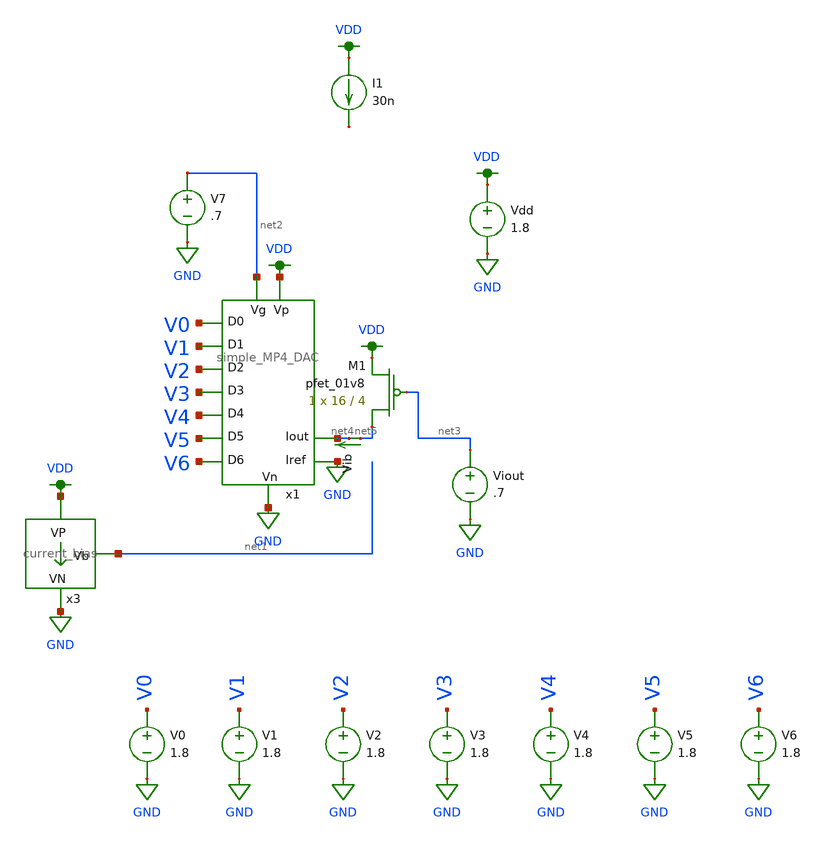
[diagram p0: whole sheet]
** sch_path: Final DAC files/schematics/simulations/DAC_mc_simulation.sch
**.subckt DAC_mc_simulation
Vdd VDD GND 1.8
V1 V1 GND 1.8
V2 V2 GND 1.8
V3 V3 GND 1.8
V4 V4 GND 1.8
V5 V5 GND 1.8
V6 V6 GND 1.8
V0 V0 GND 1.8
I1 VDD net6 30n
V7 net2 GND .7
x3 VDD net1 GND current_bias
x1 VDD GND GND V1 V0 V2 V3 V4 V5 V6 net2 net4 simple_MP4_DAC
Viout net3 GND .7
Vib net5 net4 0
.save i(vib)
XM1 net5 net3 VDD VDD sky130_fd_pr__pfet_01v8 L=4 W=16 nf=1 ad='int((nf+1)/2) * W/nf * 0.29' as='int((nf+2)/2) * W/nf * 0.29'
+ pd='2*int((nf+1)/2) * (W/nf + 0.29)' ps='2*int((nf+2)/2) * (W/nf + 0.29)' nrd='0.29 / W' nrs='0.29 / W'
+ sa=0 sb=0 sd=0 mult=1 m=1
**** begin user architecture code

.option wnflag=1
.param MC_SWITCH=1.0
.lib ~/skywater/skywater-pdk/libraries/sky130_fd_pr_ngspice/latest/models/sky130.lib.spice tt


.save all
.control
set wr_vecnames
set wr_singlescale

let Ibias_max = 31n
let Ibias = 30n
dowhile Ibias < Ibias_max
alter Ib $&Ibias

let mc_runs = 10
let run = 1
dowhile run <= mc_runs

  let code = 0
  while code < 128
    if floor(code / 1) eq 0
      let b0 = 0
    else
      let b0 = (floor(code / 1) % 2) * 1.8
    end
    if floor(code / 2) eq 0
      let b1 = 0
    else
      let b1 = (floor(code / 2) % 2) * 1.8
    end
    if floor(code / 4) eq 0
      let b2 = 0
    else
      let b2 = (floor(code / 4) % 2) * 1.8
    end
    if floor(code / 8) eq 0
      let b3 = 0
    else
      let b3 = (floor(code / 8) % 2) * 1.8
    end
    if floor(code / 16) eq 0
      let b4 = 0
    else
      let b4 = (floor(code / 16) % 2) * 1.8
    end
    if floor(code / 32) eq 0
      let b5 = 0
    else
      let b5 = (floor(code / 32) % 2) * 1.8
    end
    if floor(code / 64) eq 0
      let b6 = 0
    else
      let b6 = (floor(code / 64) % 2) * 1.8
    end

    alter V0 $&b0
    alter V1 $&b1
    alter V2 $&b2
    alter V3 $&b3
    alter V4 $&b4
    alter V5 $&b5
    alter V6 $&b6
    save all
    op

    wrdata ~/dev/git/7-bit-D-A-converter-MP4-MADVLSI/schematics/simulations/ieee_DAC/James_MC_tests_DAC/MC_files/ieeeDAC_{$&run}.txt
+ V0 V1 V2 V3 V4 V5 V6 i(Vib) i(Viout)
    if code eq 0
      set appendwrite
      set wr_vecnames = FALSE
    end
    let code = code + 1
  end
  reset
  set appendwrite = FALSE
  set wr_vecnames
  let run = run + 1
end

let Ibias = Ibias * 2
end
.endc

**** end user architecture code
**.ends
.GLOBAL VDD
.GLOBAL GND
.end
